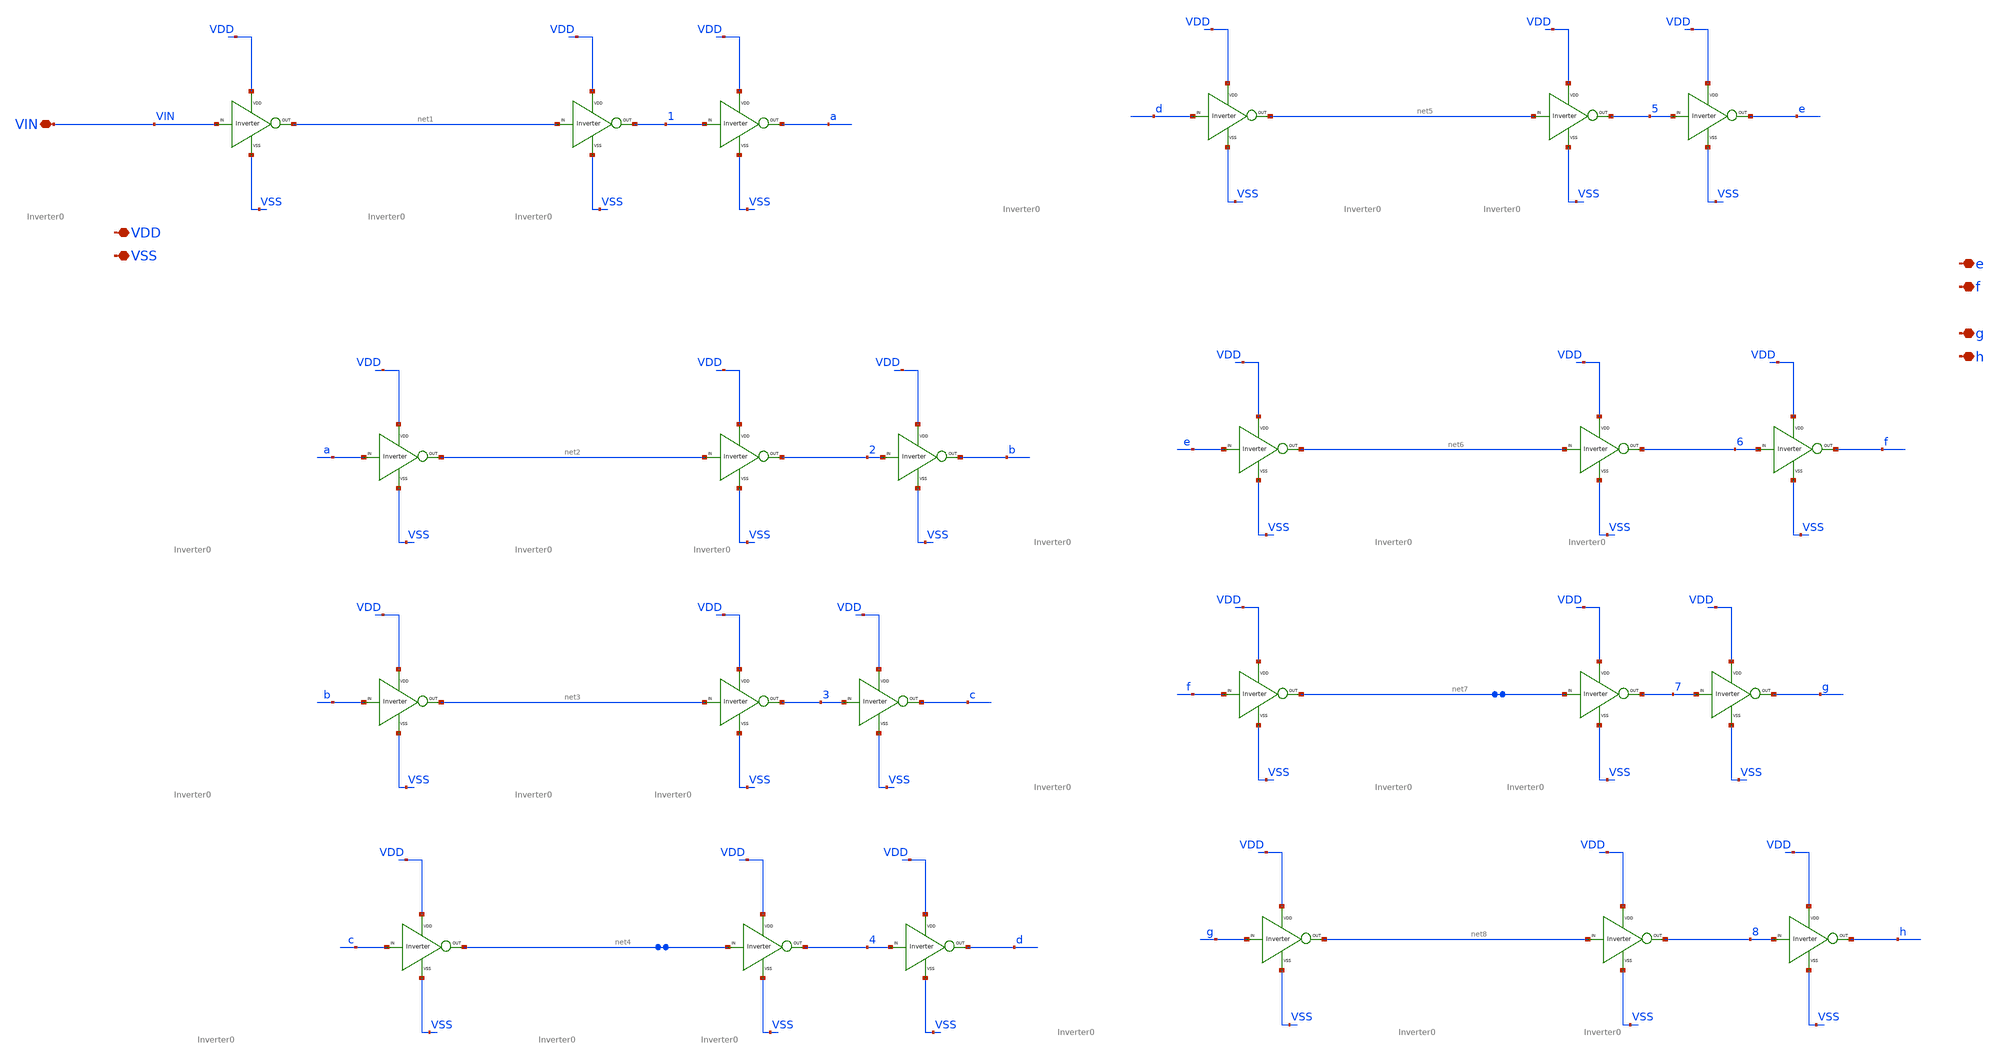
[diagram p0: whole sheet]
** sch_path: xschem/DC_DC_Converter_xschem/DC_DC_Converter/Delay_block_revised/delay1_stage2.sch
**.subckt delay1_stage2 VDD VSS VIN e f g h
*.iopin VDD
*.iopin VSS
*.iopin VIN
*.iopin e
*.iopin f
*.iopin g
*.iopin h
X13 c net4 VDD VSS Inverter0
X11 4 d VDD VSS Inverter0
X7 b net3 VDD VSS Inverter0
X9 3 c VDD VSS Inverter0
X4 a net2 VDD VSS Inverter0
X6 2 b VDD VSS Inverter0
X1 VIN net1 VDD VSS Inverter0
X3 1 a VDD VSS Inverter0
X25 net1 1 VDD VSS Inverter0
X26 net2 2 VDD VSS Inverter0
X27 net3 3 VDD VSS Inverter0
X28 net4 4 VDD VSS Inverter0
X12 d net5 VDD VSS Inverter0
X15 5 e VDD VSS Inverter0
X16 e net6 VDD VSS Inverter0
X18 6 f VDD VSS Inverter0
X19 f net7 VDD VSS Inverter0
X21 7 g VDD VSS Inverter0
X22 g net8 VDD VSS Inverter0
X24 8 h VDD VSS Inverter0
X29 net5 5 VDD VSS Inverter0
X30 net6 6 VDD VSS Inverter0
X31 net7 7 VDD VSS Inverter0
X32 net8 8 VDD VSS Inverter0
**.ends

* expanding   symbol:  DC_DC_Converter/Delay_block_revised/Inverter_0/Inverter0.sym # of pins=4
** sym_path: xschem/DC_DC_Converter_xschem/DC_DC_Converter/Delay_block_revised/Inverter_0/Inverter0.sym
** sch_path: xschem/DC_DC_Converter_xschem/DC_DC_Converter/Delay_block_revised/Inverter_0/Inverter0.sch
.subckt Inverter0 VIN VOUT VDD VSS
*.ipin VIN
*.iopin VDD
*.iopin VSS
*.opin VOUT
XM1 VOUT VIN VSS VSS sky130_fd_pr__nfet_01v8 L=0.15 W=0.4 nf=1 ad='int((nf+1)/2) * W/nf * 0.29' as='int((nf+2)/2) * W/nf * 0.29'
+ pd='2*int((nf+1)/2) * (W/nf + 0.29)' ps='2*int((nf+2)/2) * (W/nf + 0.29)' nrd='0.29 / W' nrs='0.29 / W'
+ sa=0 sb=0 sd=0 mult=1 m=1
XM2 VOUT VIN VDD VDD sky130_fd_pr__pfet_01v8 L=0.15 W=1.2 nf=1 ad='int((nf+1)/2) * W/nf * 0.29' as='int((nf+2)/2) * W/nf * 0.29'
+ pd='2*int((nf+1)/2) * (W/nf + 0.29)' ps='2*int((nf+2)/2) * (W/nf + 0.29)' nrd='0.29 / W' nrs='0.29 / W'
+ sa=0 sb=0 sd=0 mult=1 m=1
.ends

.end
